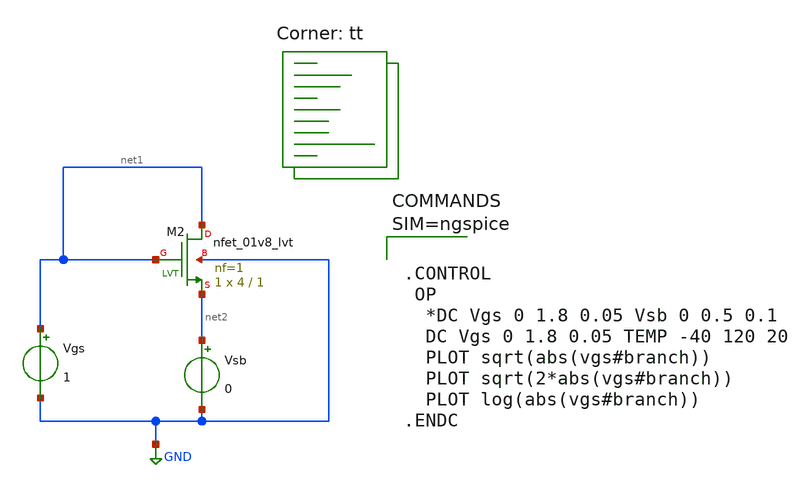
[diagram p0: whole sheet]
** sch_path: xschem_eg/id_vs_vgs_nmos.sch
**.subckt id_vs_vgs_nmos
XM2 net1 net1 net2 GND sky130_fd_pr__nfet_01v8_lvt L=1 W=4 nf=1 ad='int((1 + 1)/2) * 4 / 1 * 0.29' as='int((1 + 2)/2) * 4 / 1 * 0.29'
+ pd='2*int((1 + 1)/2) * (4 / 1 + 0.29)' ps='2*int((1 + 2)/2) * (4 / 1 + 0.29)' nrd='0.29 / 4 ' nrs='0.29 / 4 '
+ sa=0 sb=0 sd=0 mult=1 m=1
Vgs net1 GND 1
Vsb net2 GND 0
**** begin user architecture code



.CONTROL
 OP
  *DC Vgs 0 1.8 0.05 Vsb 0 0.5 0.1
  DC Vgs 0 1.8 0.05 TEMP -40 120 20
  PLOT sqrt(abs(vgs#branch))
  PLOT sqrt(2*abs(vgs#branch))
  PLOT log(abs(vgs#branch))
.ENDC



.lib $::SKYWATER_MODELS/sky130.lib.spice tt
 .lib /usr/local/share/pdk/sky130A/libs.tech/ngspice/sky130.lib.spice tt
**** end user architecture code
**.ends
.GLOBAL GND
.end
